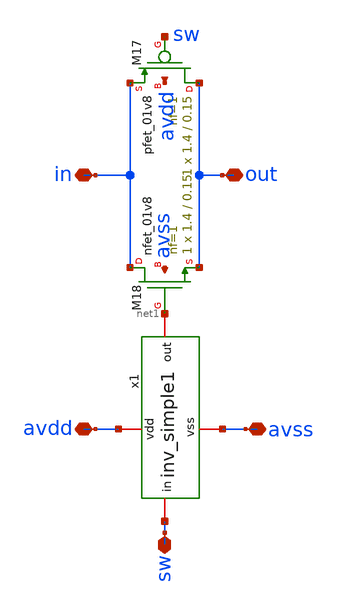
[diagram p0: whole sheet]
** sch_path: xschem/t_gate1.sch
**.subckt t_gate1 in avdd avss sw out
*.iopin in
*.iopin avdd
*.iopin avss
*.iopin sw
*.iopin out
XM17 out sw in avdd sky130_fd_pr__pfet_01v8 L=0.15 W=1.4 nf=1 ad='int((nf+1)/2) * W/nf * 0.29' as='int((nf+2)/2) * W/nf * 0.29'
+ pd='2*int((nf+1)/2) * (W/nf + 0.29)' ps='2*int((nf+2)/2) * (W/nf + 0.29)' nrd='0.29 / W' nrs='0.29 / W'
+ sa=0 sb=0 sd=0 mult=1 m=1
XM18 in net1 out avss sky130_fd_pr__nfet_01v8 L=0.15 W=1.4 nf=1 ad='int((nf+1)/2) * W/nf * 0.29' as='int((nf+2)/2) * W/nf * 0.29'
+ pd='2*int((nf+1)/2) * (W/nf + 0.29)' ps='2*int((nf+2)/2) * (W/nf + 0.29)' nrd='0.29 / W' nrs='0.29 / W'
+ sa=0 sb=0 sd=0 mult=1 m=1
x1 avdd sw net1 avss inv_simple1
**.ends

* expanding   symbol:  ma2022/inv_simple1.sym # of pins=4
** sym_path: xschem/inv_simple1.sym
** sch_path: xschem/inv_simple1.sch
.subckt inv_simple1 vdd in out vss
*.iopin in
*.iopin vdd
*.iopin vss
*.iopin out
XM19 out in vss vss sky130_fd_pr__nfet_01v8 L=0.15 W=1.4 nf=1 ad='int((nf+1)/2) * W/nf * 0.29' as='int((nf+2)/2) * W/nf * 0.29'
+ pd='2*int((nf+1)/2) * (W/nf + 0.29)' ps='2*int((nf+2)/2) * (W/nf + 0.29)' nrd='0.29 / W' nrs='0.29 / W'
+ sa=0 sb=0 sd=0 mult=1 m=1
XM20 out in vdd vdd sky130_fd_pr__pfet_01v8 L=0.15 W=2.8 nf=1 ad='int((nf+1)/2) * W/nf * 0.29' as='int((nf+2)/2) * W/nf * 0.29'
+ pd='2*int((nf+1)/2) * (W/nf + 0.29)' ps='2*int((nf+2)/2) * (W/nf + 0.29)' nrd='0.29 / W' nrs='0.29 / W'
+ sa=0 sb=0 sd=0 mult=1 m=1
XM1 vdd vdd vdd vdd sky130_fd_pr__pfet_01v8 L=0.15 W=1.4 nf=1 ad='int((nf+1)/2) * W/nf * 0.29' as='int((nf+2)/2) * W/nf * 0.29'
+ pd='2*int((nf+1)/2) * (W/nf + 0.29)' ps='2*int((nf+2)/2) * (W/nf + 0.29)' nrd='0.29 / W' nrs='0.29 / W'
+ sa=0 sb=0 sd=0 mult=1 m=1
XM2 vss vss vss vss sky130_fd_pr__nfet_01v8 L=0.15 W=1.4 nf=1 ad='int((nf+1)/2) * W/nf * 0.29' as='int((nf+2)/2) * W/nf * 0.29'
+ pd='2*int((nf+1)/2) * (W/nf + 0.29)' ps='2*int((nf+2)/2) * (W/nf + 0.29)' nrd='0.29 / W' nrs='0.29 / W'
+ sa=0 sb=0 sd=0 mult=1 m=1
.ends

.end
